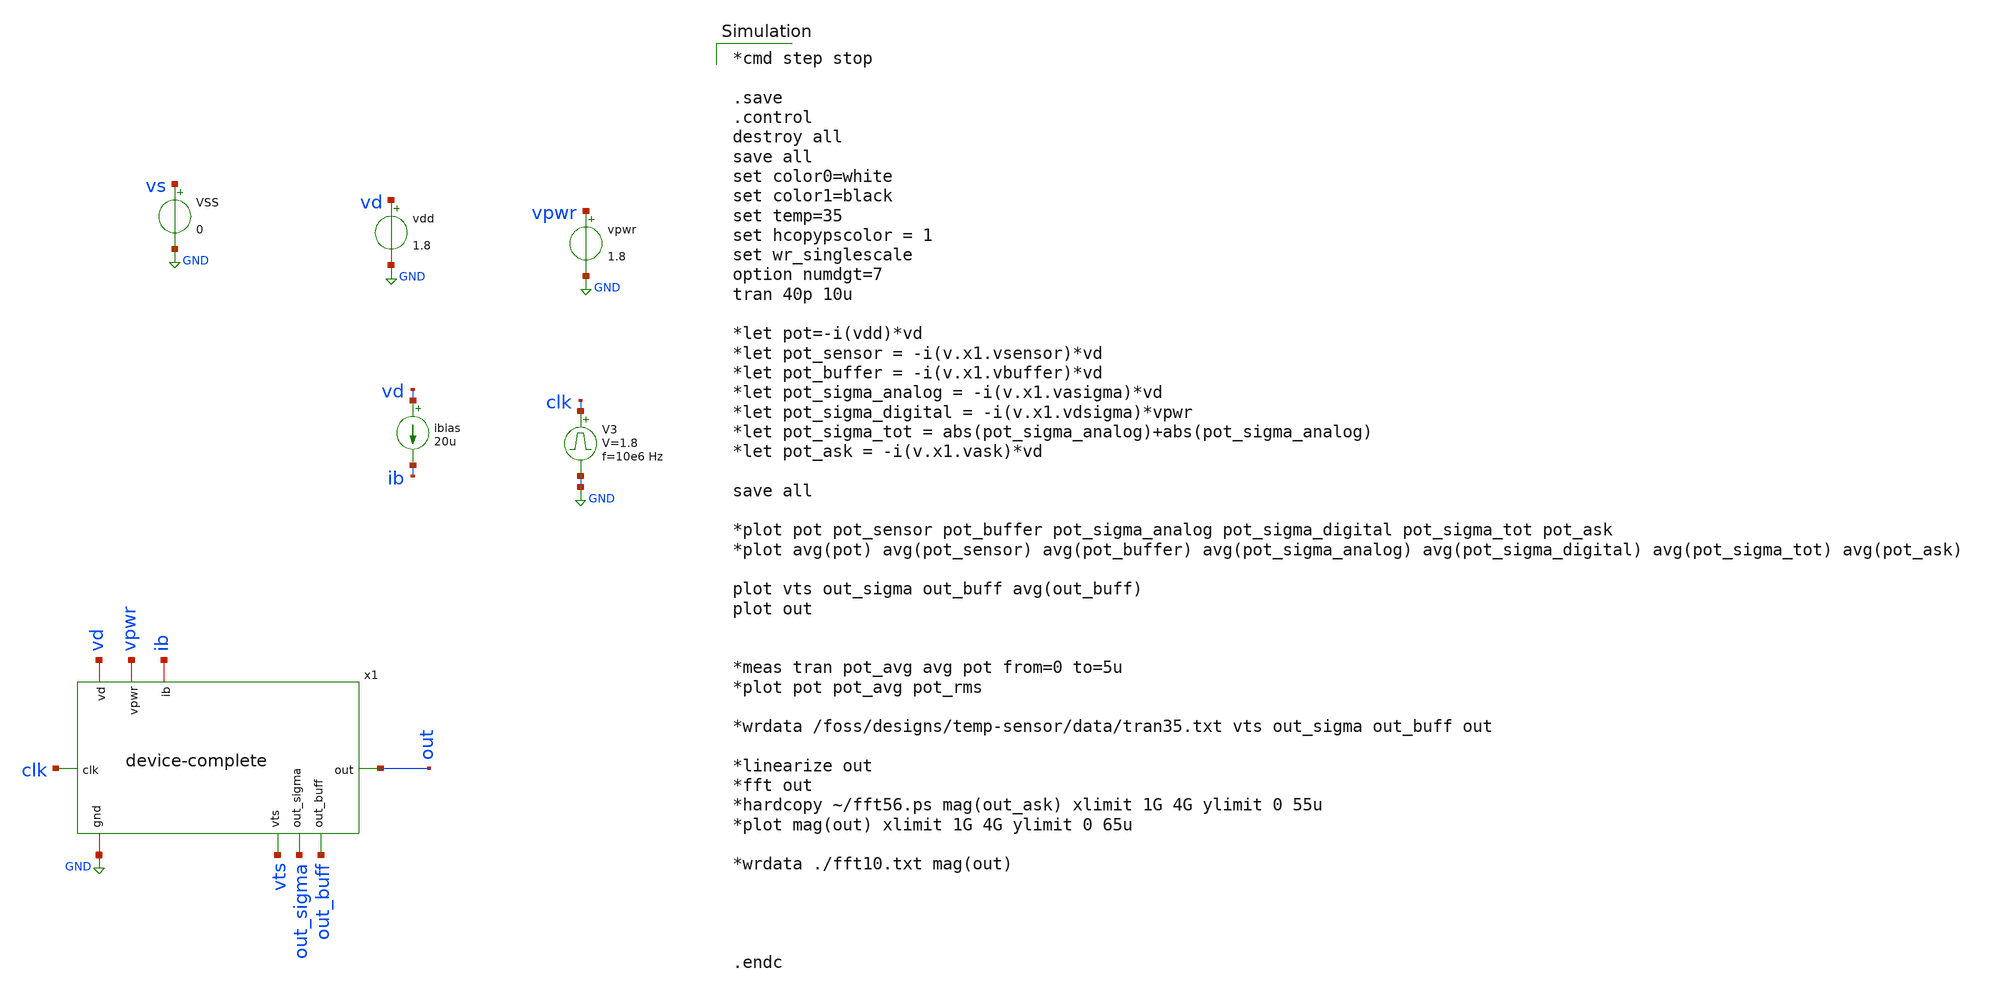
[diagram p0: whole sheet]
** sch_path: device-complete/xschem/device-complete-tb.sch
**.subckt device-complete-tb
vpwr vpwr GND 1.8
V3 clk GND pulse 0 1.8 '0.495/ 10e6 ' '0.01/10e6 ' '0.01/10e6 ' '0.49/10e6 ' '1/10e6 '
vdd vd GND 1.8
ibias vd ib 20u
VSS vs GND 0
x1 vd clk out vpwr ib GND out_buff out_sigma vts device-complete
**** begin user architecture code

*cmd step stop

.save
.control
destroy all
save all
set color0=white
set color1=black
set temp=35
set hcopypscolor = 1
set wr_singlescale
option numdgt=7
tran 40p 10u

*let pot=-i(vdd)*vd
*let pot_sensor = -i(v.x1.vsensor)*vd
*let pot_buffer = -i(v.x1.vbuffer)*vd
*let pot_sigma_analog = -i(v.x1.vasigma)*vd
*let pot_sigma_digital = -i(v.x1.vdsigma)*vpwr
*let pot_sigma_tot = abs(pot_sigma_analog)+abs(pot_sigma_analog)
*let pot_ask = -i(v.x1.vask)*vd

save all

*plot pot pot_sensor pot_buffer pot_sigma_analog pot_sigma_digital pot_sigma_tot pot_ask
*plot avg(pot) avg(pot_sensor) avg(pot_buffer) avg(pot_sigma_analog) avg(pot_sigma_digital)
*+ avg(pot_sigma_tot) avg(pot_ask)

plot vts out_sigma out_buff avg(out_buff)
plot out


*meas tran pot_avg avg pot from=0 to=5u
*plot pot pot_avg pot_rms

*wrdata /foss/designs/temp-sensor/data/tran35.txt vts out_sigma out_buff out

*linearize out
*fft out
*hardcopy ~/fft56.ps mag(out_ask) xlimit 1G 4G ylimit 0 55u
*plot mag(out) xlimit 1G 4G ylimit 0 65u

*wrdata ./fft10.txt mag(out)




.endc



 .lib $::SKYWATER_MODELS/sky130.lib.spice tt
.include $::SKYWATER_STDCELLS/sky130_fd_sc_hd.spice

**** end user architecture code
**.ends
.GLOBAL GND
.end
